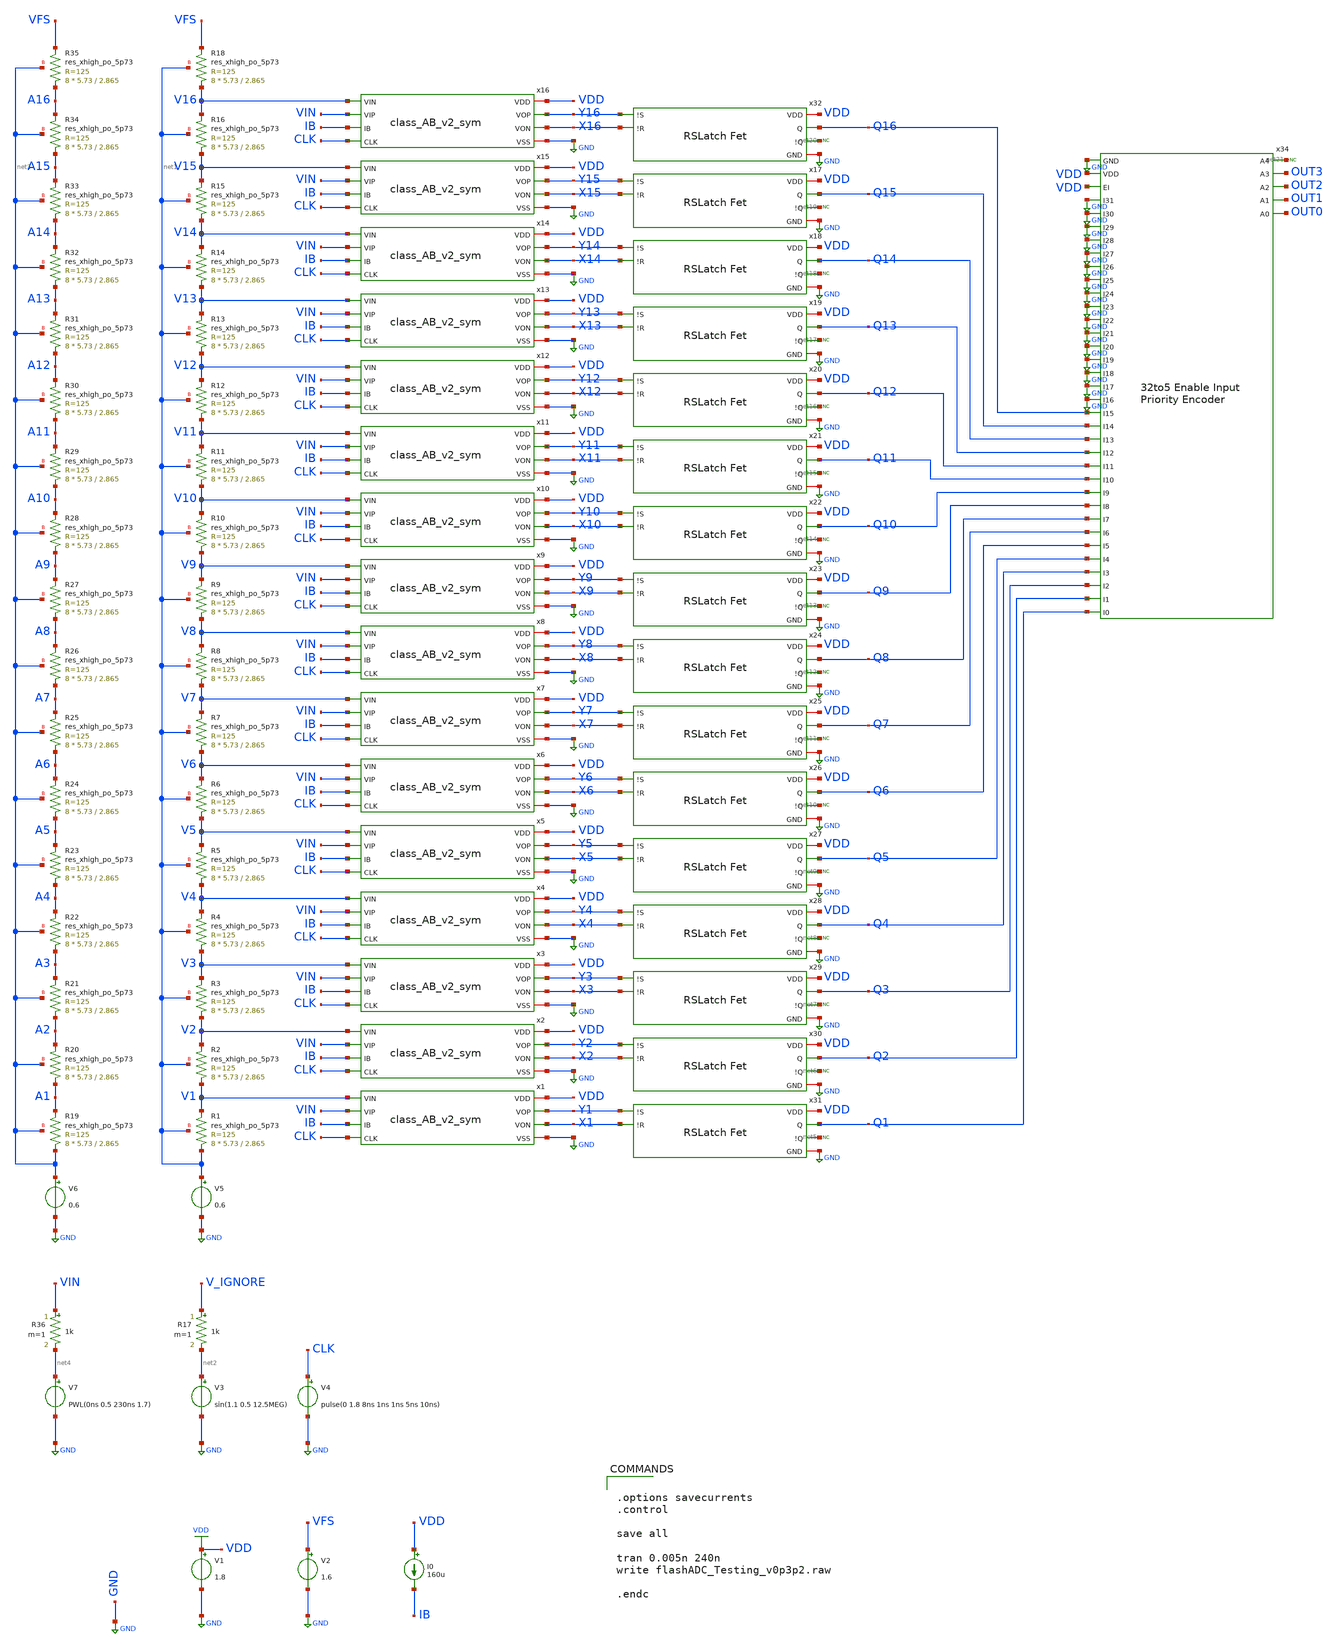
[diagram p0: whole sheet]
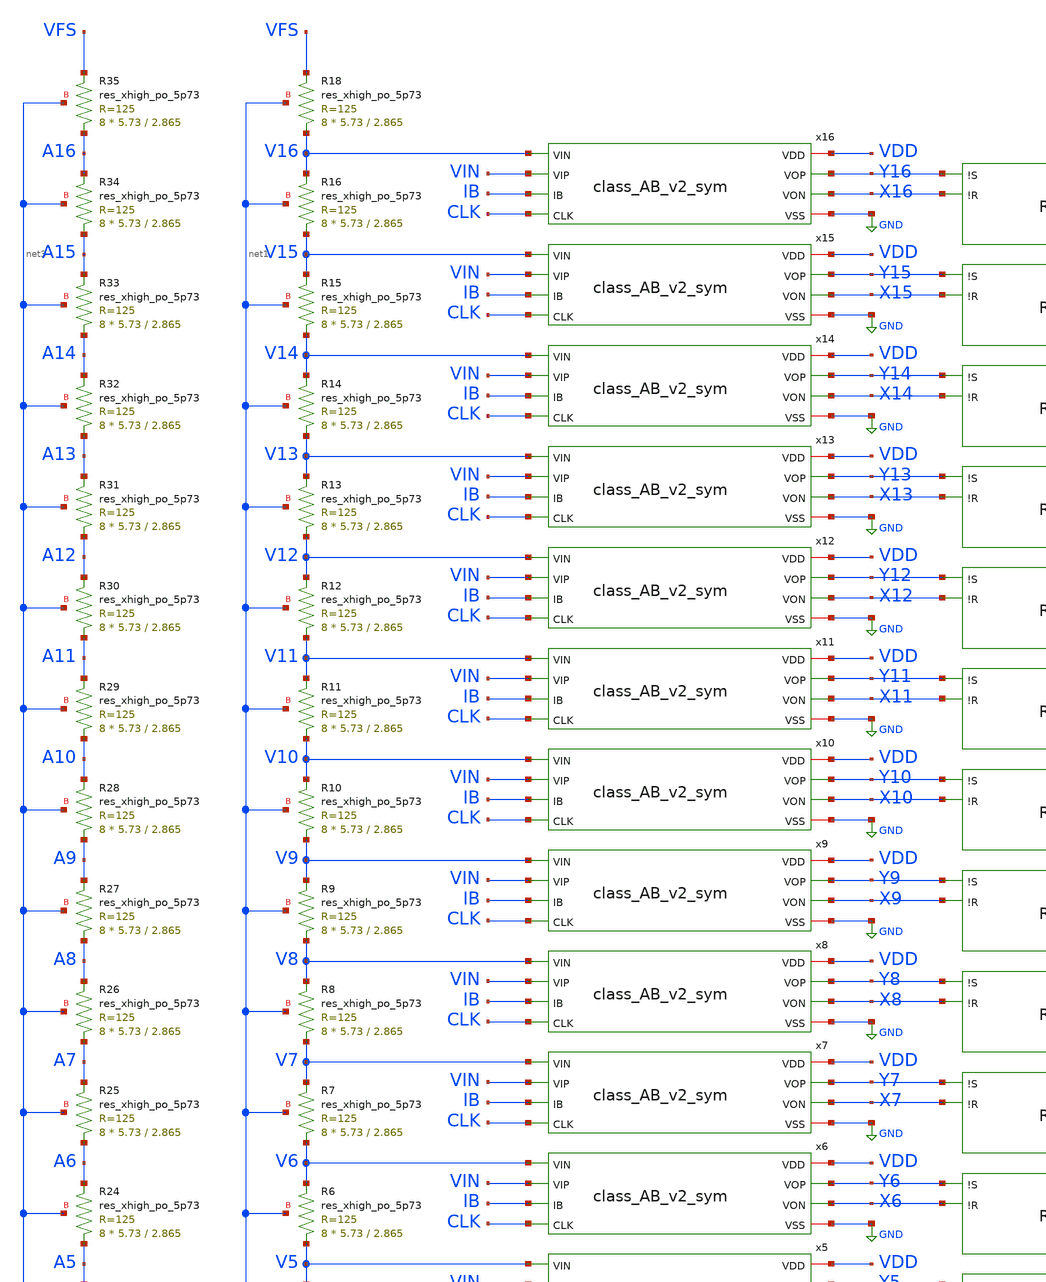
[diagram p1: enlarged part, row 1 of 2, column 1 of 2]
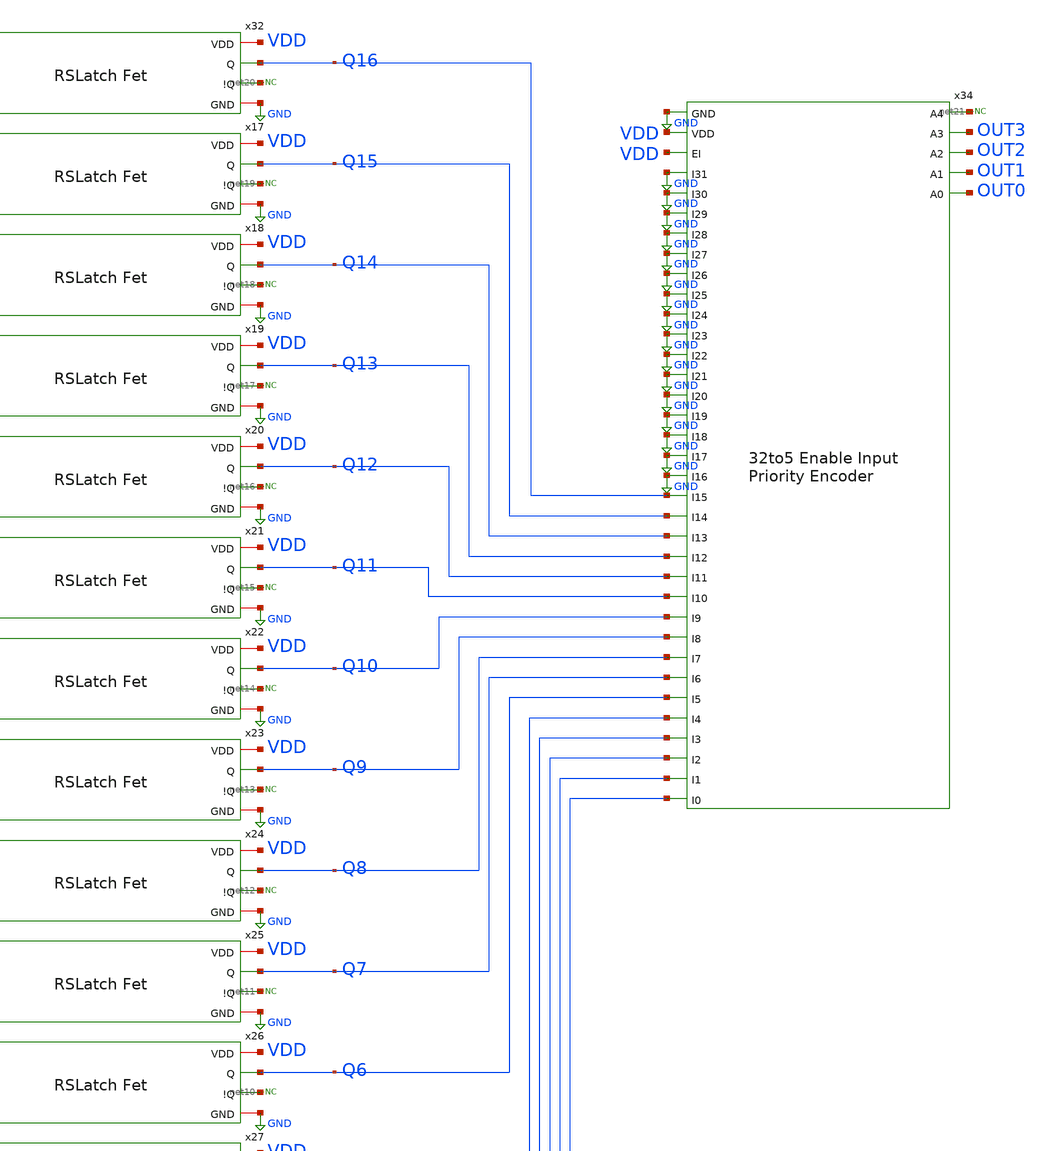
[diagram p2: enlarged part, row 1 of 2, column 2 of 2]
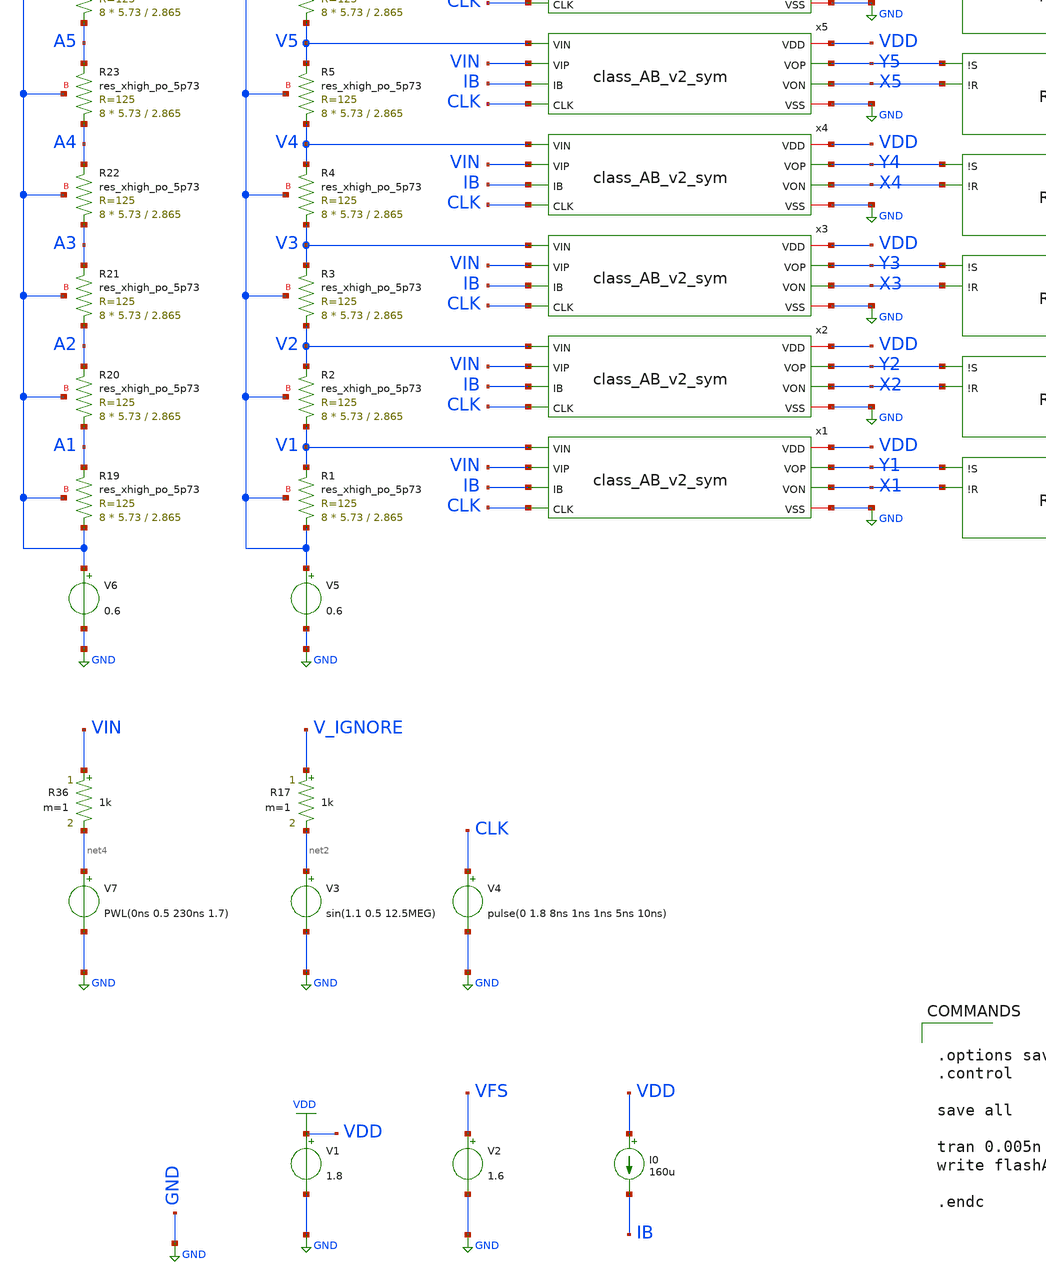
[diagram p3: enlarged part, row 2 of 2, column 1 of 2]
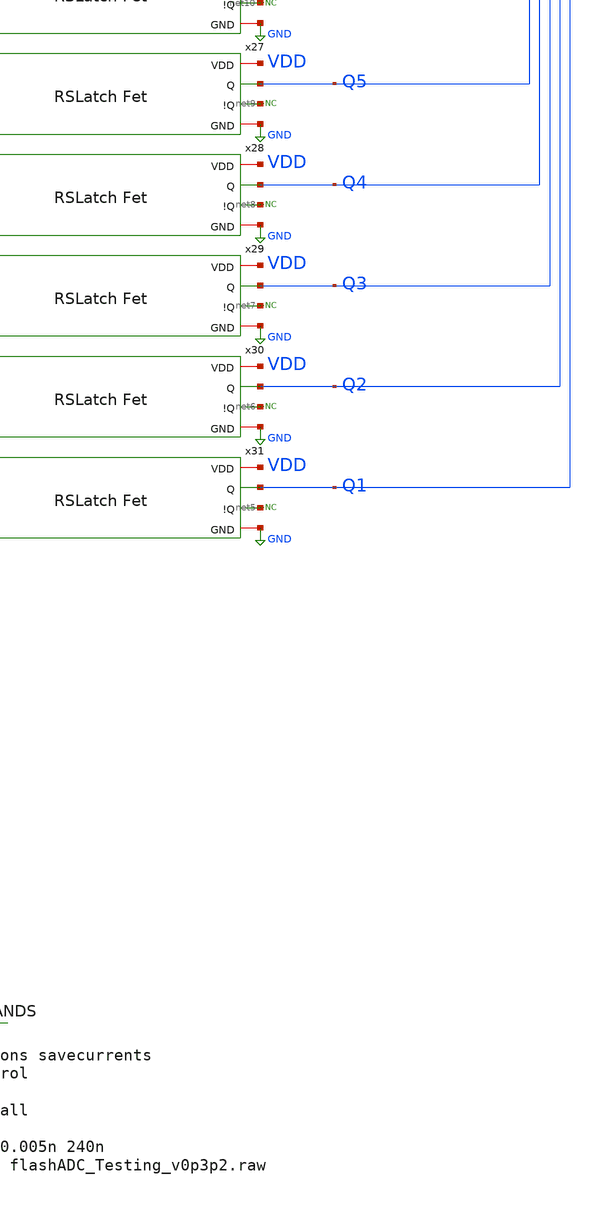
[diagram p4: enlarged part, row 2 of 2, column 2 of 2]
** sch_path: flashADC/flashADC_Testing_v0p3p2.sch
.lib $::SKYWATER_MODELS/sky130.lib.spice tt
.include $::SKYWATER_STDCELLS/sky130_fd_sc_hd.spice

**.subckt flashADC_Testing_v0p3p2
V3 net2 GND sin(1.1 0.5 12.5MEG)
V4 CLK GND pulse(0 1.8 8ns 1ns 1ns 5ns 10ns)
V1 VDD GND 1.8
V2 VFS GND 1.6
R17 V_IGNORE net2 1k m=1
I0 VDD IB 160u
V5 net1 GND 0.6
XR19 net3 A1 net3 sky130_fd_pr__res_xhigh_po_5p73 L=2.865 mult=8 m=8
V6 net3 GND 0.6
XR20 A1 A2 net3 sky130_fd_pr__res_xhigh_po_5p73 L=2.865 mult=8 m=8
XR21 A2 A3 net3 sky130_fd_pr__res_xhigh_po_5p73 L=2.865 mult=8 m=8
XR22 A3 A4 net3 sky130_fd_pr__res_xhigh_po_5p73 L=2.865 mult=8 m=8
XR23 A4 A5 net3 sky130_fd_pr__res_xhigh_po_5p73 L=2.865 mult=8 m=8
XR24 A5 A6 net3 sky130_fd_pr__res_xhigh_po_5p73 L=2.865 mult=8 m=8
XR25 A6 A7 net3 sky130_fd_pr__res_xhigh_po_5p73 L=2.865 mult=8 m=8
XR26 A7 A8 net3 sky130_fd_pr__res_xhigh_po_5p73 L=2.865 mult=8 m=8
XR27 A8 A9 net3 sky130_fd_pr__res_xhigh_po_5p73 L=2.865 mult=8 m=8
XR28 A9 A10 net3 sky130_fd_pr__res_xhigh_po_5p73 L=2.865 mult=8 m=8
XR29 A10 A11 net3 sky130_fd_pr__res_xhigh_po_5p73 L=2.865 mult=8 m=8
XR30 A11 A12 net3 sky130_fd_pr__res_xhigh_po_5p73 L=2.865 mult=8 m=8
XR31 A12 A13 net3 sky130_fd_pr__res_xhigh_po_5p73 L=2.865 mult=8 m=8
XR32 A13 A14 net3 sky130_fd_pr__res_xhigh_po_5p73 L=2.865 mult=8 m=8
XR33 A14 A15 net3 sky130_fd_pr__res_xhigh_po_5p73 L=2.865 mult=8 m=8
XR34 A15 A16 net3 sky130_fd_pr__res_xhigh_po_5p73 L=2.865 mult=8 m=8
XR35 A16 VFS net3 sky130_fd_pr__res_xhigh_po_5p73 L=2.865 mult=8 m=8
XR1 net1 V1 net1 sky130_fd_pr__res_xhigh_po_5p73 L=2.865 mult=8 m=8
XR2 V1 V2 net1 sky130_fd_pr__res_xhigh_po_5p73 L=2.865 mult=8 m=8
XR3 V2 V3 net1 sky130_fd_pr__res_xhigh_po_5p73 L=2.865 mult=8 m=8
XR4 V3 V4 net1 sky130_fd_pr__res_xhigh_po_5p73 L=2.865 mult=8 m=8
XR5 V4 V5 net1 sky130_fd_pr__res_xhigh_po_5p73 L=2.865 mult=8 m=8
XR6 V5 V6 net1 sky130_fd_pr__res_xhigh_po_5p73 L=2.865 mult=8 m=8
XR7 V6 V7 net1 sky130_fd_pr__res_xhigh_po_5p73 L=2.865 mult=8 m=8
XR8 V7 V8 net1 sky130_fd_pr__res_xhigh_po_5p73 L=2.865 mult=8 m=8
XR9 V8 V9 net1 sky130_fd_pr__res_xhigh_po_5p73 L=2.865 mult=8 m=8
XR10 V9 V10 net1 sky130_fd_pr__res_xhigh_po_5p73 L=2.865 mult=8 m=8
XR11 V10 V11 net1 sky130_fd_pr__res_xhigh_po_5p73 L=2.865 mult=8 m=8
XR12 V11 V12 net1 sky130_fd_pr__res_xhigh_po_5p73 L=2.865 mult=8 m=8
XR13 V12 V13 net1 sky130_fd_pr__res_xhigh_po_5p73 L=2.865 mult=8 m=8
XR14 V13 V14 net1 sky130_fd_pr__res_xhigh_po_5p73 L=2.865 mult=8 m=8
XR15 V14 V15 net1 sky130_fd_pr__res_xhigh_po_5p73 L=2.865 mult=8 m=8
XR16 V15 V16 net1 sky130_fd_pr__res_xhigh_po_5p73 L=2.865 mult=8 m=8
XR18 V16 VFS net1 sky130_fd_pr__res_xhigh_po_5p73 L=2.865 mult=8 m=8
V7 net4 GND PWL(0ns 0.5 230ns 1.7)
R36 VIN net4 1k m=1
x1 VDD Y1 X1 V1 VIN IB CLK GND class_AB_v2_sym
x2 VDD Y2 X2 V2 VIN IB CLK GND class_AB_v2_sym
x3 VDD Y3 X3 V3 VIN IB CLK GND class_AB_v2_sym
x4 VDD Y4 X4 V4 VIN IB CLK GND class_AB_v2_sym
x5 VDD Y5 X5 V5 VIN IB CLK GND class_AB_v2_sym
x6 VDD Y6 X6 V6 VIN IB CLK GND class_AB_v2_sym
x7 VDD Y7 X7 V7 VIN IB CLK GND class_AB_v2_sym
x8 VDD Y8 X8 V8 VIN IB CLK GND class_AB_v2_sym
x9 VDD Y9 X9 V9 VIN IB CLK GND class_AB_v2_sym
x10 VDD Y10 X10 V10 VIN IB CLK GND class_AB_v2_sym
x11 VDD Y11 X11 V11 VIN IB CLK GND class_AB_v2_sym
x12 VDD Y12 X12 V12 VIN IB CLK GND class_AB_v2_sym
x13 VDD Y13 X13 V13 VIN IB CLK GND class_AB_v2_sym
x14 VDD Y14 X14 V14 VIN IB CLK GND class_AB_v2_sym
x15 VDD Y15 X15 V15 VIN IB CLK GND class_AB_v2_sym
x16 VDD Y16 X16 V16 VIN IB CLK GND class_AB_v2_sym
* noconn #net5
* noconn #net6
* noconn #net7
* noconn #net8
* noconn #net9
* noconn #net10
* noconn #net11
* noconn #net12
* noconn #net13
* noconn #net14
* noconn #net15
* noconn #net16
* noconn #net17
* noconn #net18
* noconn #net19
* noconn #net20
* noconn #net21
x32 VDD Y16 X16 Q16 net20 GND RSfetsym
x17 VDD Y15 X15 Q15 net19 GND RSfetsym
x18 VDD Y14 X14 Q14 net18 GND RSfetsym
x19 VDD Y13 X13 Q13 net17 GND RSfetsym
x20 VDD Y12 X12 Q12 net16 GND RSfetsym
x21 VDD Y11 X11 Q11 net15 GND RSfetsym
x22 VDD Y10 X10 Q10 net14 GND RSfetsym
x23 VDD Y9 X9 Q9 net13 GND RSfetsym
x24 VDD Y8 X8 Q8 net12 GND RSfetsym
x25 VDD Y7 X7 Q7 net11 GND RSfetsym
x26 VDD Y6 X6 Q6 net10 GND RSfetsym
x27 VDD Y5 X5 Q5 net9 GND RSfetsym
x28 VDD Y4 X4 Q4 net8 GND RSfetsym
x29 VDD Y3 X3 Q3 net7 GND RSfetsym
x30 VDD Y2 X2 Q2 net6 GND RSfetsym
x31 VDD Y1 X1 Q1 net5 GND RSfetsym
x34 GND VDD VDD net21 GND GND GND GND GND GND GND GND OUT3 GND GND GND GND GND GND GND GND OUT2 Q16
+ Q15 Q14 Q13 Q12 Q11 Q10 OUT1 Q9 Q8 Q7 Q6 Q5 OUT0 Q4 Q3 Q2 Q1 32to5_Priority_Encoder_v0p2p1
**** begin user architecture code


.options savecurrents
.control

save all

tran 0.005n 240n
write flashADC_Testing_v0p3p2.raw

.endc


**** end user architecture code
**.ends
.GLOBAL GND
.GLOBAL VDD
.end
